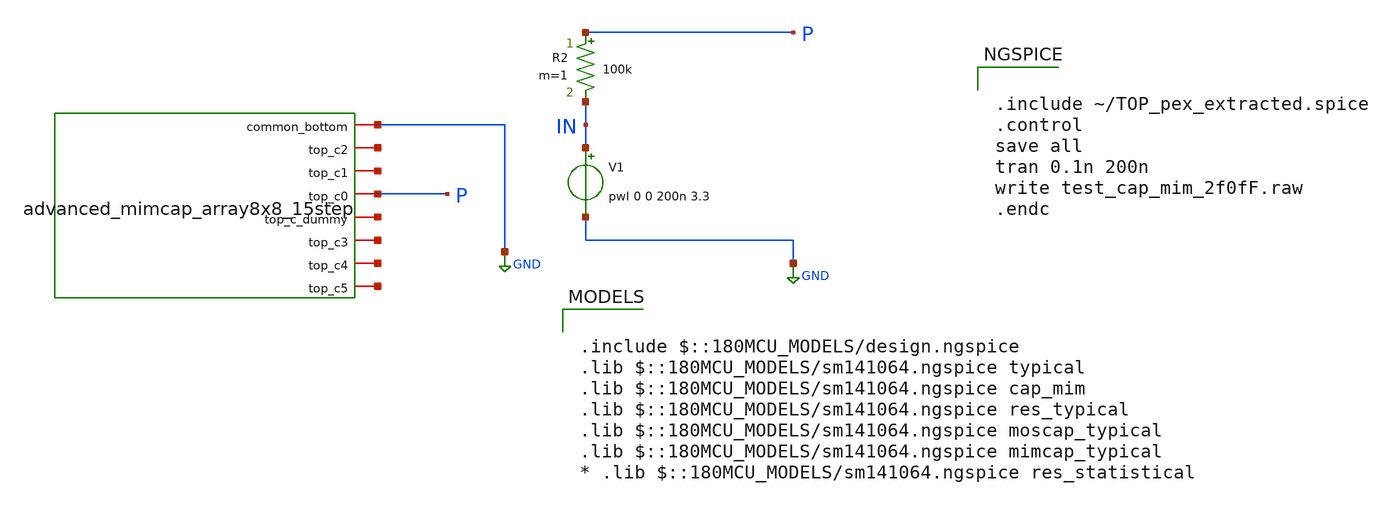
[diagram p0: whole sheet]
** sch_path: cdac/mim_cap_array_8x8/tb/test_cap_mim_2f0fF.sch
* Copyright 2022 GlobalFoundries PDK Authors
* Licensed under the Apache License, Version 2.0 (the "License");
* you may not use this file except in compliance with the License.
* You may obtain a copy of the License at
* https://www.apache.org/licenses/LICENSE-2.0
* Unless required by applicable law or agreed to in writing, software
* distributed under the License is distributed on an "AS IS" BASIS,
* WITHOUT WARRANTIES OR CONDITIONS OF ANY KIND, either express or implied.
* See the License for the specific language governing permissions and
* limitations under the License.
**.subckt test_cap_mim_2f0fF
V1 IN GND pwl 0 0 200n 3.3
R2 P IN 100k m=1
x1 P net2 net6 net4 net1 net5 net3 GND TOP
**** begin user architecture code

.include $::180MCU_MODELS/design.ngspice
.lib $::180MCU_MODELS/sm141064.ngspice typical
.lib $::180MCU_MODELS/sm141064.ngspice cap_mim
.lib $::180MCU_MODELS/sm141064.ngspice res_typical
.lib $::180MCU_MODELS/sm141064.ngspice moscap_typical
.lib $::180MCU_MODELS/sm141064.ngspice mimcap_typical
* .lib $::180MCU_MODELS/sm141064.ngspice res_statistical



.include ~/TOP_pex_extracted.spice
.control
save all
tran 0.1n 200n
write test_cap_mim_2f0fF.raw
.endc


**** end user architecture code
**.ends
.GLOBAL GND
.end
